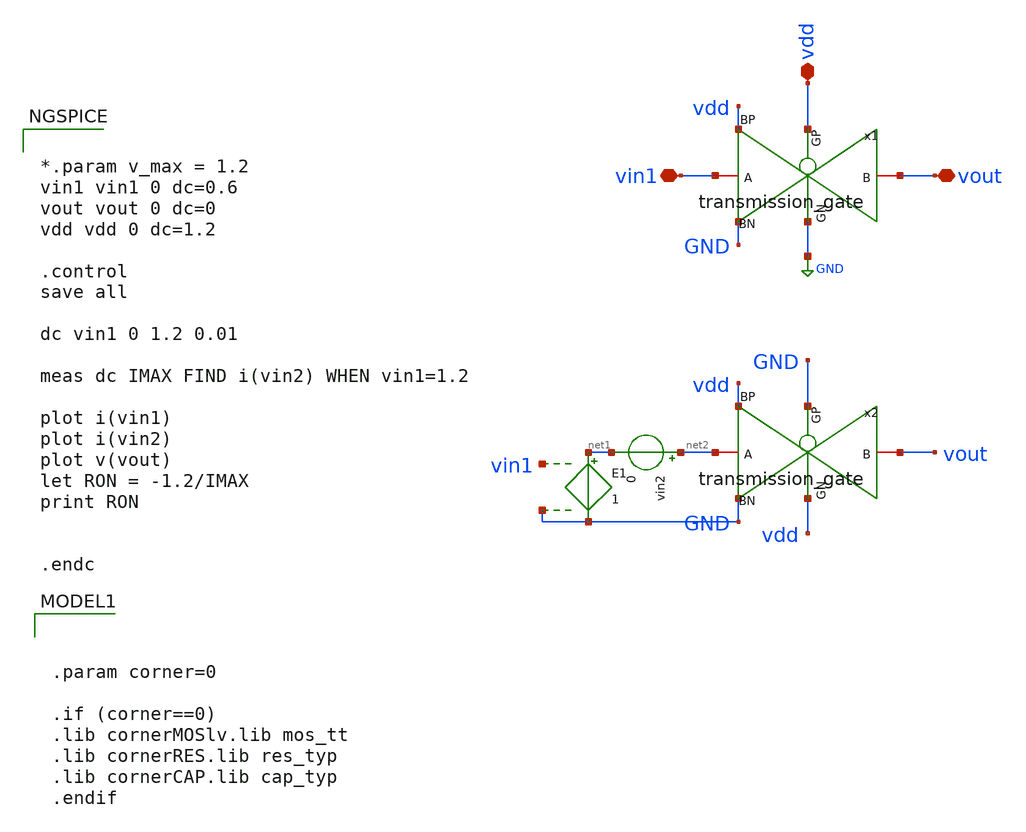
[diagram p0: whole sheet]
** sch_path: others/tb_transmission_gate.sch
**.subckt tb_transmission_gate vin1 vout vdd
*.iopin vin1
*.iopin vout
*.iopin vdd
E1 net1 GND vin1 GND 1
vin2 net2 net1 0
x1 vout GND vdd vin1 vdd GND transmission_gate
x2 vout vdd GND net2 vdd GND transmission_gate
**** begin user architecture code


*.param v_max = 1.2
vin1 vin1 0 dc=0.6
vout vout 0 dc=0
vdd vdd 0 dc=1.2

.control
save all

dc vin1 0 1.2 0.01

meas dc IMAX FIND i(vin2) WHEN vin1=1.2

plot i(vin1)
plot i(vin2)
plot v(vout)
let RON = -1.2/IMAX
print RON


.endc




.param corner=0

.if (corner==0)
.lib cornerMOSlv.lib mos_tt
.lib cornerRES.lib res_typ
.lib cornerCAP.lib cap_typ
.endif

**** end user architecture code
**.ends

* expanding   symbol:  /foss/designs/DLL/others/transmission_gate.sym # of pins=6
** sym_path: DelayLine/others/transmission_gate.sym
** sch_path: DelayLine/others/transmission_gate.sch
.subckt transmission_gate B GN GP A BP BN
*.iopin B
*.iopin GN
*.iopin A
*.iopin GP
*.iopin BN
*.iopin BP
XM1 A GN B BN sg13_lv_nmos w=1 l=0.13u ng=4 m=1 mm_ok=1
XM2 A GP B BP sg13_lv_pmos w=1 l=0.13u ng=4 m=1 mm_ok=1
.ends

.GLOBAL GND
.end
